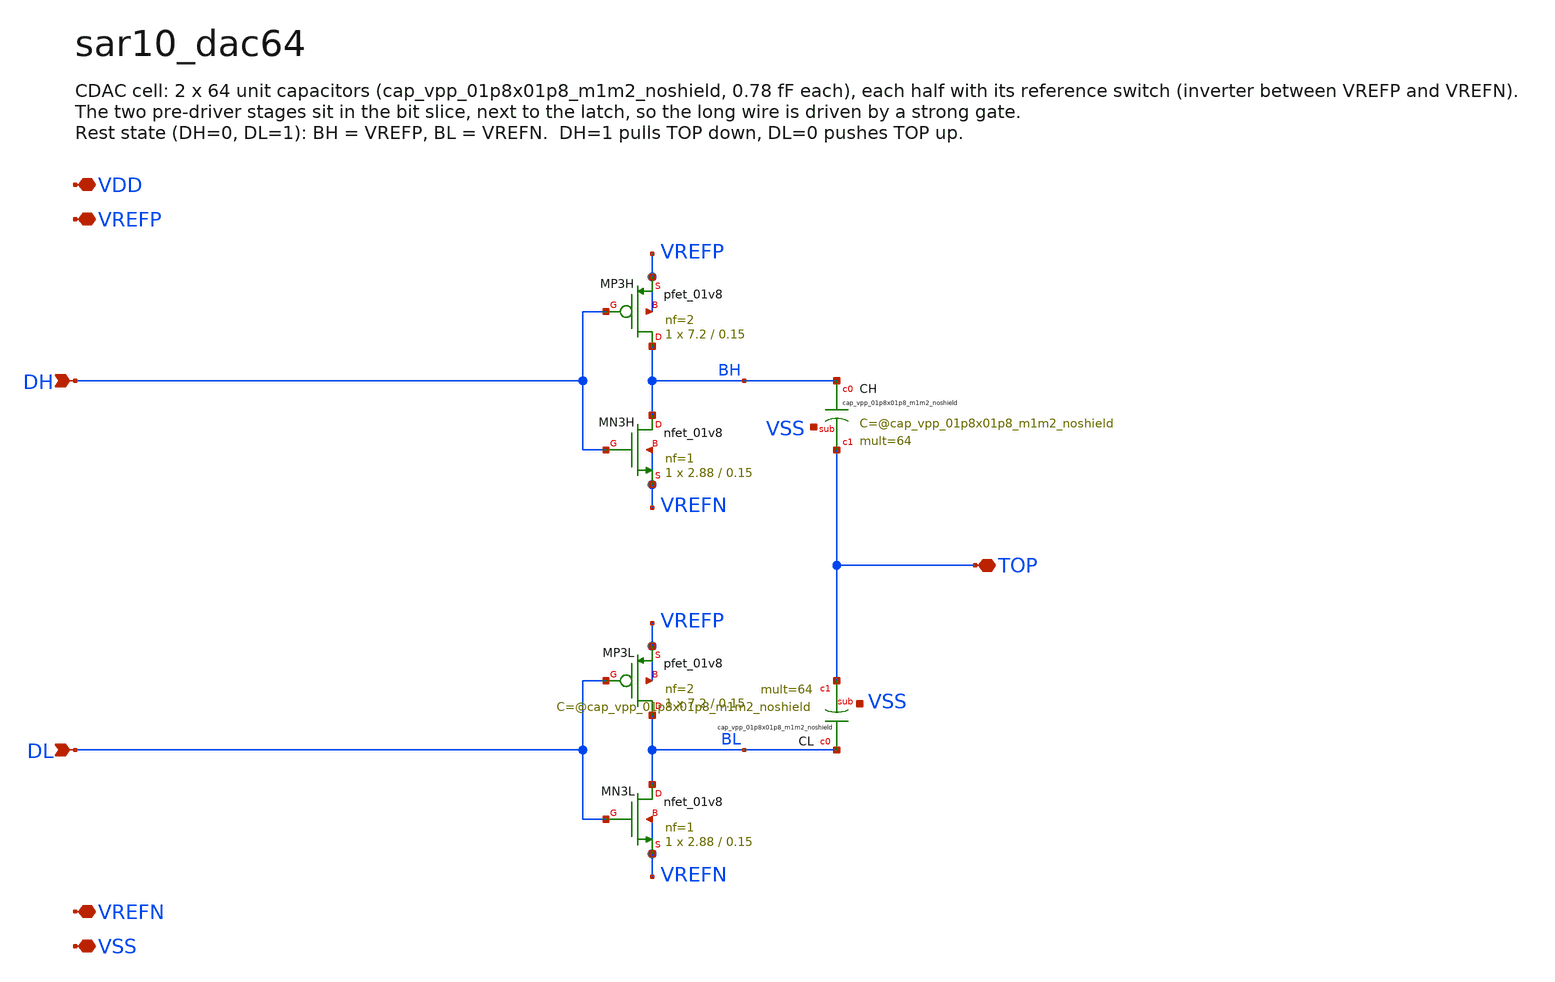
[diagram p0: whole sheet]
** sch_path: xschem/sar10_dac64.sch
**.subckt sar10_dac64 DH DL TOP VDD VREFP VREFN VSS
*.ipin DH
*.ipin DL
*.iopin TOP
*.iopin VDD
*.iopin VREFP
*.iopin VREFN
*.iopin VSS
XMP3H BH DH VREFP VREFP sky130_fd_pr__pfet_01v8 L=0.15 W=7.2 nf=2 ad='int((2 + 1)/2) * 7.2 / 2 * 0.29'
+ as='int((2 + 2)/2) * 7.2 / 2 * 0.29' pd='2*int((2 + 1)/2) * (7.2 / 2 + 0.29)' ps='2*int((2 + 2)/2) * (7.2 / 2 + 0.29)'
+ nrd='0.29 / 7.2 ' nrs='0.29 / 7.2 ' sa=0 sb=0 sd=0 mult=1 m=1
XMN3H BH DH VREFN VREFN sky130_fd_pr__nfet_01v8 L=0.15 W=2.88 nf=1 ad='int((1 + 1)/2) * 2.88 / 1 * 0.29'
+ as='int((1 + 2)/2) * 2.88 / 1 * 0.29' pd='2*int((1 + 1)/2) * (2.88 / 1 + 0.29)' ps='2*int((1 + 2)/2) * (2.88 / 1 + 0.29)'
+ nrd='0.29 / 2.88 ' nrs='0.29 / 2.88 ' sa=0 sb=0 sd=0 mult=1 m=1
XMP3L BL DL VREFP VREFP sky130_fd_pr__pfet_01v8 L=0.15 W=7.2 nf=2 ad='int((2 + 1)/2) * 7.2 / 2 * 0.29'
+ as='int((2 + 2)/2) * 7.2 / 2 * 0.29' pd='2*int((2 + 1)/2) * (7.2 / 2 + 0.29)' ps='2*int((2 + 2)/2) * (7.2 / 2 + 0.29)'
+ nrd='0.29 / 7.2 ' nrs='0.29 / 7.2 ' sa=0 sb=0 sd=0 mult=1 m=1
XMN3L BL DL VREFN VREFN sky130_fd_pr__nfet_01v8 L=0.15 W=2.88 nf=1 ad='int((1 + 1)/2) * 2.88 / 1 * 0.29'
+ as='int((1 + 2)/2) * 2.88 / 1 * 0.29' pd='2*int((1 + 1)/2) * (2.88 / 1 + 0.29)' ps='2*int((1 + 2)/2) * (2.88 / 1 + 0.29)'
+ nrd='0.29 / 2.88 ' nrs='0.29 / 2.88 ' sa=0 sb=0 sd=0 mult=1 m=1
XCH BH TOP VSS sky130_fd_pr__cap_vpp_01p8x01p8_m1m2_noshield mult=64 m=64
XCL BL TOP VSS sky130_fd_pr__cap_vpp_01p8x01p8_m1m2_noshield mult=64 m=64
**.ends
.end
